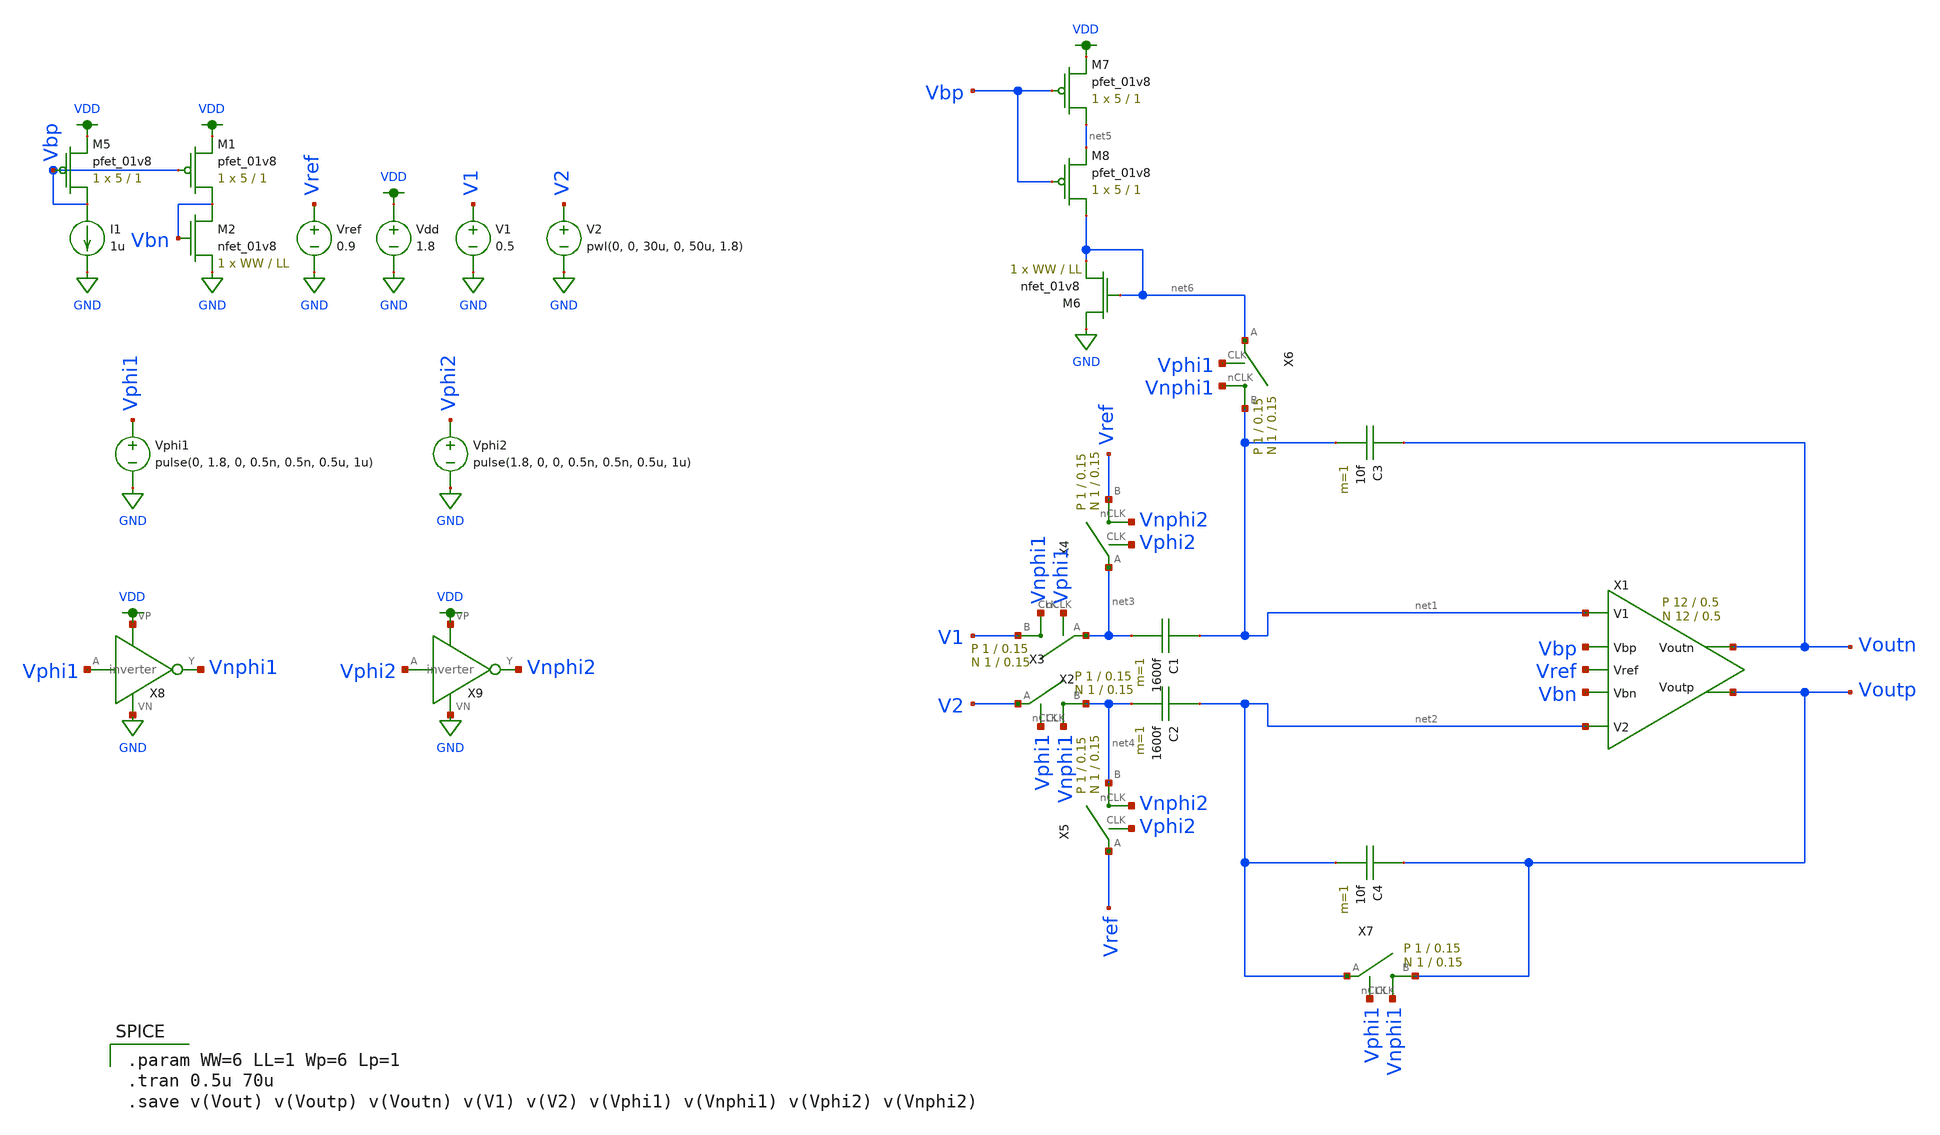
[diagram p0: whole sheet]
** sch_path: schematic/FG_diffamp_full_swing_test.sch
**.subckt FG_diffamp_full_swing_test
X1 net1 net2 Voutp Voutn Vbp Vref Vbn fully_differential_sc_amp Wp=12 Lp=0.5 WW=12 LL=0.5
C1 net1 net3 1600f m=1
C2 net2 net4 1600f m=1
C3 Voutn net1 10f m=1
C4 Voutp net2 10f m=1
X2 V1 net3 Vphi1 Vnphi1 switch Wp=1 Lp=0.15 WW=1 LL=0.15
X3 net4 V2 Vphi1 Vnphi1 switch Wp=1 Lp=0.15 WW=1 LL=0.15
X4 Vref net3 Vphi2 Vnphi2 switch Wp=1 Lp=0.15 WW=1 LL=0.15
X5 net4 Vref Vphi2 Vnphi2 switch Wp=1 Lp=0.15 WW=1 LL=0.15
X6 net1 net6 Vphi1 Vnphi1 switch Wp=1 Lp=0.15 WW=1 LL=0.15
X7 Voutp net2 Vphi1 Vnphi1 switch Wp=1 Lp=0.15 WW=1 LL=0.15
XM7 net5 Vbp VDD VDD sky130_fd_pr__pfet_01v8 L=1 W=5 nf=1 ad='int((nf+1)/2) * W/nf * 0.29' as='int((nf+2)/2) * W/nf * 0.29'
+ pd='2*int((nf+1)/2) * (W/nf + 0.29)' ps='2*int((nf+2)/2) * (W/nf + 0.29)' nrd='0.29 / W' nrs='0.29 / W'
+ sa=0 sb=0 sd=0 mult=1 m=1
XM8 net6 Vbp net5 VDD sky130_fd_pr__pfet_01v8 L=1 W=5 nf=1 ad='int((nf+1)/2) * W/nf * 0.29' as='int((nf+2)/2) * W/nf * 0.29'
+ pd='2*int((nf+1)/2) * (W/nf + 0.29)' ps='2*int((nf+2)/2) * (W/nf + 0.29)' nrd='0.29 / W' nrs='0.29 / W'
+ sa=0 sb=0 sd=0 mult=1 m=1
XM6 GND net6 net6 GND sky130_fd_pr__nfet_01v8 L=LL W=WW nf=1 ad='int((nf+1)/2) * W/nf * 0.29' as='int((nf+2)/2) * W/nf * 0.29'
+ pd='2*int((nf+1)/2) * (W/nf + 0.29)' ps='2*int((nf+2)/2) * (W/nf + 0.29)' nrd='0.29 / W' nrs='0.29 / W'
+ sa=0 sb=0 sd=0 mult=1 m=1
Vdd VDD GND 1.8
V1 V1 GND 0.5
V2 V2 GND pwl(0, 0, 30u, 0, 50u, 1.8)
Vphi1 Vphi1 GND pulse(0, 1.8, 0, 0.5n, 0.5n, 0.5u, 1u)
X8 Vphi1 Vnphi1 VDD GND inverter
Vphi2 Vphi2 GND pulse(1.8, 0, 0, 0.5n, 0.5n, 0.5u, 1u)
X9 Vphi2 Vnphi2 VDD GND inverter
Vref Vref GND 0.9
XM5 Vbp Vbp VDD VDD sky130_fd_pr__pfet_01v8 L=1 W=5 nf=1 ad='int((nf+1)/2) * W/nf * 0.29' as='int((nf+2)/2) * W/nf * 0.29'
+ pd='2*int((nf+1)/2) * (W/nf + 0.29)' ps='2*int((nf+2)/2) * (W/nf + 0.29)' nrd='0.29 / W' nrs='0.29 / W'
+ sa=0 sb=0 sd=0 mult=1 m=1
I1 Vbp GND 1u
XM1 Vbn Vbp VDD VDD sky130_fd_pr__pfet_01v8 L=1 W=5 nf=1 ad='int((nf+1)/2) * W/nf * 0.29' as='int((nf+2)/2) * W/nf * 0.29'
+ pd='2*int((nf+1)/2) * (W/nf + 0.29)' ps='2*int((nf+2)/2) * (W/nf + 0.29)' nrd='0.29 / W' nrs='0.29 / W'
+ sa=0 sb=0 sd=0 mult=1 m=1
XM2 Vbn Vbn GND GND sky130_fd_pr__nfet_01v8 L=LL W=WW nf=1 ad='int((nf+1)/2) * W/nf * 0.29' as='int((nf+2)/2) * W/nf * 0.29'
+ pd='2*int((nf+1)/2) * (W/nf + 0.29)' ps='2*int((nf+2)/2) * (W/nf + 0.29)' nrd='0.29 / W' nrs='0.29 / W'
+ sa=0 sb=0 sd=0 mult=1 m=1
**** begin user architecture code

.option wnflag=1
.param MC_SWITCH=0.0
.lib ~/skywater/skywater-pdk/libraries/sky130_fd_pr_ngspice/latest/models/sky130.lib.spice tt


.param WW=6 LL=1 Wp=6 Lp=1
.tran 0.5u 70u
.save v(Vout) v(Voutp) v(Voutn) v(V1) v(V2) v(Vphi1) v(Vnphi1) v(Vphi2) v(Vnphi2)

**** end user architecture code
**.ends

* expanding   symbol:
*+  /home/madvlsi/Documents/MADVLSI-Final_Project/schematic/fully_differential_sc_amp.sym # of pins=7
** sym_path: schematic/archive/fully_differential_sc_amp.sym
** sch_path: schematic/archive/fully_differential_sc_amp.sch
.subckt fully_differential_sc_amp V1 V2 Voutp Voutn Vbp Vref Vbn  Wp=1 Lp=0.15 WW=1 LL=0.15
*.ipin V1
*.ipin V2
*.ipin Vbp
*.ipin Vbn
*.ipin Vref
*.iopin Voutp
*.iopin Voutn
XM1a net2 V1 GND GND sky130_fd_pr__nfet_01v8 L=LL W=WW nf=1 ad='int((nf+1)/2) * W/nf * 0.29' as='int((nf+2)/2) * W/nf * 0.29'
+ pd='2*int((nf+1)/2) * (W/nf + 0.29)' ps='2*int((nf+2)/2) * (W/nf + 0.29)' nrd='0.29 / W' nrs='0.29 / W'
+ sa=0 sb=0 sd=0 mult=1 m=1
XM1b Voutn V1 GND GND sky130_fd_pr__nfet_01v8 L=LL W=WW nf=1 ad='int((nf+1)/2) * W/nf * 0.29' as='int((nf+2)/2) * W/nf * 0.29'
+ pd='2*int((nf+1)/2) * (W/nf + 0.29)' ps='2*int((nf+2)/2) * (W/nf + 0.29)' nrd='0.29 / W' nrs='0.29 / W'
+ sa=0 sb=0 sd=0 mult=1 m=1
XM2b Voutp V2 GND GND sky130_fd_pr__nfet_01v8 L=LL W=WW nf=1 ad='int((nf+1)/2) * W/nf * 0.29' as='int((nf+2)/2) * W/nf * 0.29'
+ pd='2*int((nf+1)/2) * (W/nf + 0.29)' ps='2*int((nf+2)/2) * (W/nf + 0.29)' nrd='0.29 / W' nrs='0.29 / W'
+ sa=0 sb=0 sd=0 mult=1 m=1
XM2a net2 V2 GND GND sky130_fd_pr__nfet_01v8 L=LL W=WW nf=1 ad='int((nf+1)/2) * W/nf * 0.29' as='int((nf+2)/2) * W/nf * 0.29'
+ pd='2*int((nf+1)/2) * (W/nf + 0.29)' ps='2*int((nf+2)/2) * (W/nf + 0.29)' nrd='0.29 / W' nrs='0.29 / W'
+ sa=0 sb=0 sd=0 mult=1 m=1
XMb net2 Vbp VDD VDD sky130_fd_pr__pfet_01v8 L=Lp W=Wp nf=1 ad='int((nf+1)/2) * W/nf * 0.29' as='int((nf+2)/2) * W/nf * 0.29'
+ pd='2*int((nf+1)/2) * (W/nf + 0.29)' ps='2*int((nf+2)/2) * (W/nf + 0.29)' nrd='0.29 / W' nrs='0.29 / W'
+ sa=0 sb=0 sd=0 mult=1 m=1
C2b net2 V2 1600f m=1
C2a net2 V1 1600f m=1
XM1 GND V2 net1 GND sky130_fd_pr__nfet_01v8 L=LL W=WW nf=1 ad='int((nf+1)/2) * W/nf * 0.29' as='int((nf+2)/2) * W/nf * 0.29'
+ pd='2*int((nf+1)/2) * (W/nf + 0.29)' ps='2*int((nf+2)/2) * (W/nf + 0.29)' nrd='0.29 / W' nrs='0.29 / W'
+ sa=0 sb=0 sd=0 mult=1 m=1
XM2 GND V1 net1 GND sky130_fd_pr__nfet_01v8 L=LL W=WW nf=1 ad='int((nf+1)/2) * W/nf * 0.29' as='int((nf+2)/2) * W/nf * 0.29'
+ pd='2*int((nf+1)/2) * (W/nf + 0.29)' ps='2*int((nf+2)/2) * (W/nf + 0.29)' nrd='0.29 / W' nrs='0.29 / W'
+ sa=0 sb=0 sd=0 mult=1 m=1
XMb1 VDD net4 net5 VDD sky130_fd_pr__pfet_01v8 L=Lp W=Wp nf=1 ad='int((nf+1)/2) * W/nf * 0.29' as='int((nf+2)/2) * W/nf * 0.29'
+ pd='2*int((nf+1)/2) * (W/nf + 0.29)' ps='2*int((nf+2)/2) * (W/nf + 0.29)' nrd='0.29 / W' nrs='0.29 / W'
+ sa=0 sb=0 sd=0 mult=1 m=1
XMb2 VDD net4 net1 VDD sky130_fd_pr__pfet_01v8 L=Lp W=Wp nf=1 ad='int((nf+1)/2) * W/nf * 0.29' as='int((nf+2)/2) * W/nf * 0.29'
+ pd='2*int((nf+1)/2) * (W/nf + 0.29)' ps='2*int((nf+2)/2) * (W/nf + 0.29)' nrd='0.29 / W' nrs='0.29 / W'
+ sa=0 sb=0 sd=0 mult=1 m=1
XMb4 VDD net4 net6 VDD sky130_fd_pr__pfet_01v8 L=Lp W=Wp nf=1 ad='int((nf+1)/2) * W/nf * 0.29' as='int((nf+2)/2) * W/nf * 0.29'
+ pd='2*int((nf+1)/2) * (W/nf + 0.29)' ps='2*int((nf+2)/2) * (W/nf + 0.29)' nrd='0.29 / W' nrs='0.29 / W'
+ sa=0 sb=0 sd=0 mult=1 m=1
XMb5 net7 net4 VDD VDD sky130_fd_pr__pfet_01v8 L=Lp W=Wp nf=1 ad='int((nf+1)/2) * W/nf * 0.29' as='int((nf+2)/2) * W/nf * 0.29'
+ pd='2*int((nf+1)/2) * (W/nf + 0.29)' ps='2*int((nf+2)/2) * (W/nf + 0.29)' nrd='0.29 / W' nrs='0.29 / W'
+ sa=0 sb=0 sd=0 mult=1 m=1
XM3 net3 Vbn GND GND sky130_fd_pr__nfet_01v8 L=LL W=WW nf=1 ad='int((nf+1)/2) * W/nf * 0.29' as='int((nf+2)/2) * W/nf * 0.29'
+ pd='2*int((nf+1)/2) * (W/nf + 0.29)' ps='2*int((nf+2)/2) * (W/nf + 0.29)' nrd='0.29 / W' nrs='0.29 / W'
+ sa=0 sb=0 sd=0 mult=1 m=1
XM4 VDD net1 net3 GND sky130_fd_pr__nfet_01v8 L=LL W=WW nf=1 ad='int((nf+1)/2) * W/nf * 0.29' as='int((nf+2)/2) * W/nf * 0.29'
+ pd='2*int((nf+1)/2) * (W/nf + 0.29)' ps='2*int((nf+2)/2) * (W/nf + 0.29)' nrd='0.29 / W' nrs='0.29 / W'
+ sa=0 sb=0 sd=0 mult=1 m=1
XM5 net3 Vref net4 GND sky130_fd_pr__nfet_01v8 L=LL W=WW nf=1 ad='int((nf+1)/2) * W/nf * 0.29' as='int((nf+2)/2) * W/nf * 0.29'
+ pd='2*int((nf+1)/2) * (W/nf + 0.29)' ps='2*int((nf+2)/2) * (W/nf + 0.29)' nrd='0.29 / W' nrs='0.29 / W'
+ sa=0 sb=0 sd=0 mult=1 m=1
XMb6 net5 net4 Voutn VDD sky130_fd_pr__pfet_01v8 L=Lp W=Wp nf=1 ad='int((nf+1)/2) * W/nf * 0.29' as='int((nf+2)/2) * W/nf * 0.29'
+ pd='2*int((nf+1)/2) * (W/nf + 0.29)' ps='2*int((nf+2)/2) * (W/nf + 0.29)' nrd='0.29 / W' nrs='0.29 / W'
+ sa=0 sb=0 sd=0 mult=1 m=1
XMb7 net6 net4 Voutp VDD sky130_fd_pr__pfet_01v8 L=Lp W=Wp nf=1 ad='int((nf+1)/2) * W/nf * 0.29' as='int((nf+2)/2) * W/nf * 0.29'
+ pd='2*int((nf+1)/2) * (W/nf + 0.29)' ps='2*int((nf+2)/2) * (W/nf + 0.29)' nrd='0.29 / W' nrs='0.29 / W'
+ sa=0 sb=0 sd=0 mult=1 m=1
XMb8 net4 net4 net7 VDD sky130_fd_pr__pfet_01v8 L=Lp W=Wp nf=1 ad='int((nf+1)/2) * W/nf * 0.29' as='int((nf+2)/2) * W/nf * 0.29'
+ pd='2*int((nf+1)/2) * (W/nf + 0.29)' ps='2*int((nf+2)/2) * (W/nf + 0.29)' nrd='0.29 / W' nrs='0.29 / W'
+ sa=0 sb=0 sd=0 mult=1 m=1
.ends


* expanding   symbol:  /home/madvlsi/Documents/MADVLSI-Final_Project/schematic/switch.sym # of
*+ pins=4
** sym_path: schematic/switch.sym
** sch_path: schematic/switch.sch
.subckt switch B A CLK nCLK  Wp=1 Lp=0.15 WW=1 LL=0.15
*.iopin B
*.iopin A
*.ipin CLK
*.ipin nCLK
*.ipin CLK
*.ipin CLK
*.ipin nCLK
*.ipin nCLK
XM1 A CLK B GND sky130_fd_pr__nfet_01v8 L={LL} W={WW} nf=1 ad='int((nf+1)/2) * W/nf * 0.29' as='int((nf+2)/2) * W/nf * 0.29'
+ pd='2*int((nf+1)/2) * (W/nf + 0.29)' ps='2*int((nf+2)/2) * (W/nf + 0.29)' nrd='0.29 / W' nrs='0.29 / W'
+ sa=0 sb=0 sd=0 mult=1 m=1
XM2 A nCLK B VDD sky130_fd_pr__pfet_01v8 L={Lp} W={Wp} nf=1 ad='int((nf+1)/2) * W/nf * 0.29' as='int((nf+2)/2) * W/nf * 0.29'
+ pd='2*int((nf+1)/2) * (W/nf + 0.29)' ps='2*int((nf+2)/2) * (W/nf + 0.29)' nrd='0.29 / W' nrs='0.29 / W'
+ sa=0 sb=0 sd=0 mult=1 m=1
XM3 B CLK B VDD sky130_fd_pr__pfet_01v8 L={Lp} W={Wp/2} nf=1 ad='int((nf+1)/2) * W/nf * 0.29' as='int((nf+2)/2) * W/nf * 0.29'
+ pd='2*int((nf+1)/2) * (W/nf + 0.29)' ps='2*int((nf+2)/2) * (W/nf + 0.29)' nrd='0.29 / W' nrs='0.29 / W'
+ sa=0 sb=0 sd=0 mult=1 m=1
XM4 A CLK A VDD sky130_fd_pr__pfet_01v8 L={Lp} W={Wp/2} nf=1 ad='int((nf+1)/2) * W/nf * 0.29' as='int((nf+2)/2) * W/nf * 0.29'
+ pd='2*int((nf+1)/2) * (W/nf + 0.29)' ps='2*int((nf+2)/2) * (W/nf + 0.29)' nrd='0.29 / W' nrs='0.29 / W'
+ sa=0 sb=0 sd=0 mult=1 m=1
XM5 B nCLK B GND sky130_fd_pr__nfet_01v8 L={LL} W={WW/2} nf=1 ad='int((nf+1)/2) * W/nf * 0.29' as='int((nf+2)/2) * W/nf * 0.29'
+ pd='2*int((nf+1)/2) * (W/nf + 0.29)' ps='2*int((nf+2)/2) * (W/nf + 0.29)' nrd='0.29 / W' nrs='0.29 / W'
+ sa=0 sb=0 sd=0 mult=1 m=1
XM6 A nCLK A GND sky130_fd_pr__nfet_01v8 L={LL} W={WW/2} nf=1 ad='int((nf+1)/2) * W/nf * 0.29' as='int((nf+2)/2) * W/nf * 0.29'
+ pd='2*int((nf+1)/2) * (W/nf + 0.29)' ps='2*int((nf+2)/2) * (W/nf + 0.29)' nrd='0.29 / W' nrs='0.29 / W'
+ sa=0 sb=0 sd=0 mult=1 m=1
.ends


* expanding   symbol:  /home/madvlsi/Documents/MADVLSI-Final_Project/schematic/inverter.sym # of
*+ pins=4
** sym_path: schematic/inverter.sym
** sch_path: schematic/inverter.sch
.subckt inverter A Y VP VN
*.opin Y
*.ipin A
*.iopin VP
*.iopin VN
XM3 Y A VP VDD sky130_fd_pr__pfet_01v8 L={Lp} W={Wp} nf=1 ad='int((nf+1)/2) * W/nf * 0.29' as='int((nf+2)/2) * W/nf * 0.29'
+ pd='2*int((nf+1)/2) * (W/nf + 0.29)' ps='2*int((nf+2)/2) * (W/nf + 0.29)' nrd='0.29 / W' nrs='0.29 / W'
+ sa=0 sb=0 sd=0 mult=1 m=1
XM4 Y A VP VDD sky130_fd_pr__pfet_01v8 L={Lp} W={Wp} nf=1 ad='int((nf+1)/2) * W/nf * 0.29' as='int((nf+2)/2) * W/nf * 0.29'
+ pd='2*int((nf+1)/2) * (W/nf + 0.29)' ps='2*int((nf+2)/2) * (W/nf + 0.29)' nrd='0.29 / W' nrs='0.29 / W'
+ sa=0 sb=0 sd=0 mult=1 m=1
XM5 Y A VN GND sky130_fd_pr__nfet_01v8 L={Lp} W={Wp} nf=1 ad='int((nf+1)/2) * W/nf * 0.29' as='int((nf+2)/2) * W/nf * 0.29'
+ pd='2*int((nf+1)/2) * (W/nf + 0.29)' ps='2*int((nf+2)/2) * (W/nf + 0.29)' nrd='0.29 / W' nrs='0.29 / W'
+ sa=0 sb=0 sd=0 mult=1 m=1
.ends

.GLOBAL VDD
.GLOBAL GND
.end
